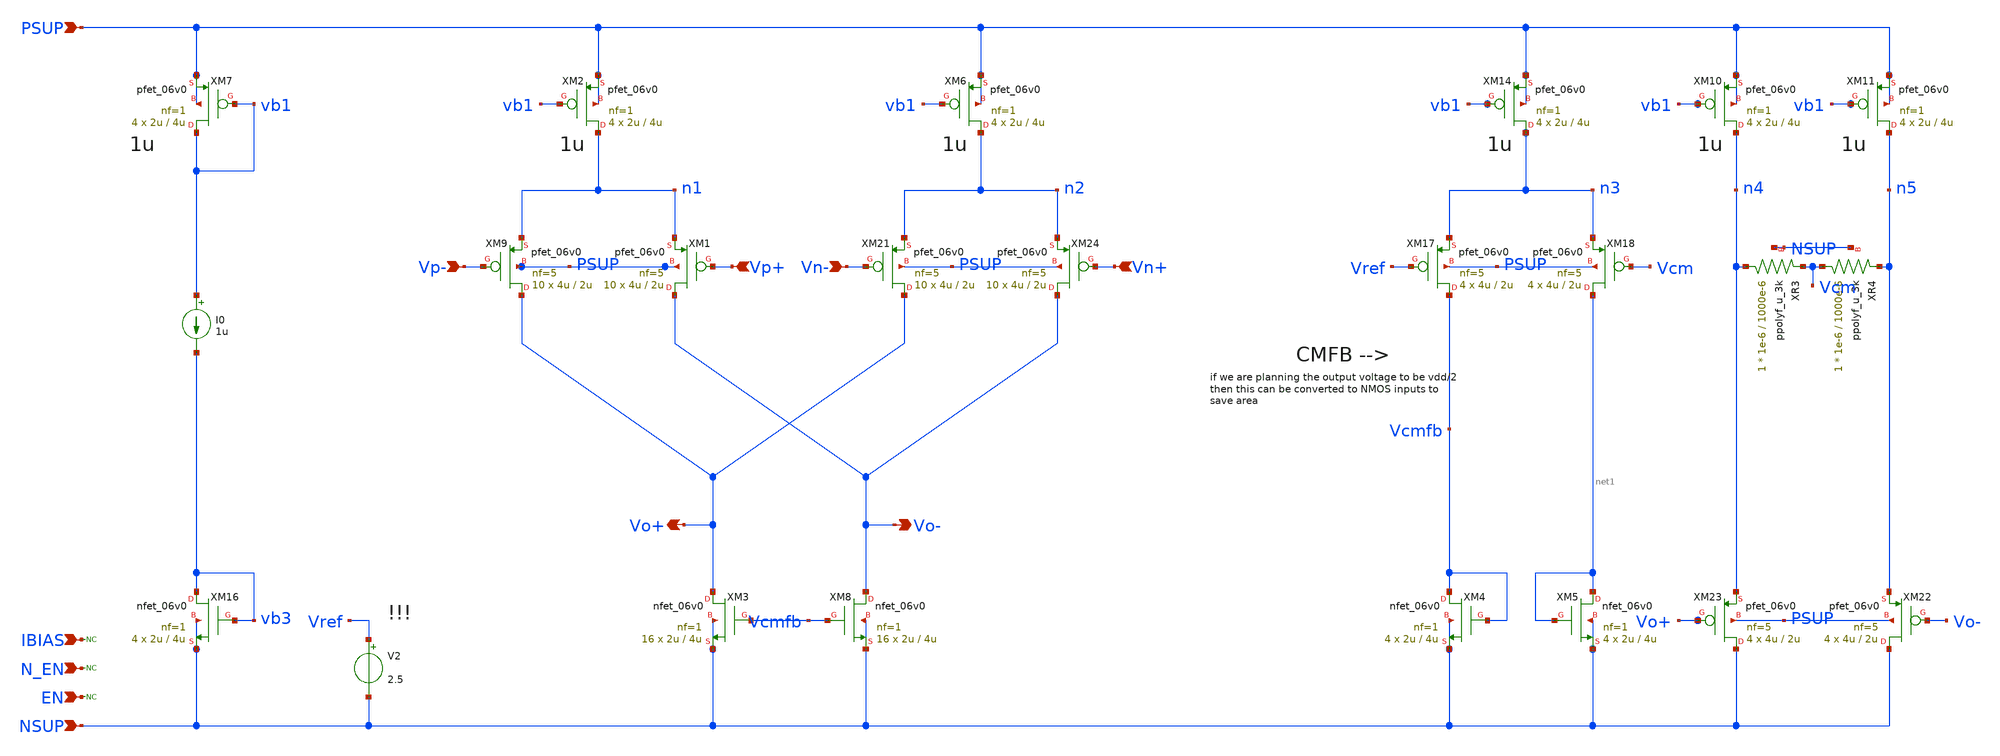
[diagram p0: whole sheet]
** sch_path: xschem/blocks/fdda/junk/fdda_no_casc.sch
**.subckt fdda_no_casc PSUP NSUP N_EN EN IBIAS Vp+ Vp- Vn+ Vn- Vo- Vo+
*.ipin PSUP
*.ipin NSUP
*.ipin N_EN
*.ipin EN
*.ipin IBIAS
*.ipin Vp+
*.ipin Vp-
*.ipin Vn+
*.ipin Vn-
*.opin Vo-
*.opin Vo+
* noconn N_EN
* noconn EN
I0 vb1 vb3 1u
XM7 vb1 vb1 PSUP PSUP pfet_06v0 L=4u W=2u nf=1 ad='int((nf+1)/2) * W/nf * 0.18u' as='int((nf+2)/2) * W/nf * 0.18u'
+ pd='2*int((nf+1)/2) * (W/nf + 0.18u)' ps='2*int((nf+2)/2) * (W/nf + 0.18u)' nrd='0.18u / W' nrs='0.18u / W'
+ sa=0 sb=0 sd=0 m=4
* noconn IBIAS
XM16 vb3 vb3 NSUP NSUP nfet_06v0 L=4u W=2u nf=1 ad='int((nf+1)/2) * W/nf * 0.18u' as='int((nf+2)/2) * W/nf * 0.18u'
+ pd='2*int((nf+1)/2) * (W/nf + 0.18u)' ps='2*int((nf+2)/2) * (W/nf + 0.18u)' nrd='0.18u / W' nrs='0.18u / W'
+ sa=0 sb=0 sd=0 m=4
V2 Vref NSUP 2.5
XM22 NSUP Vo- n5 PSUP pfet_06v0 L=2u W=4u nf=5 ad='int((nf+1)/2) * W/nf * 0.18u' as='int((nf+2)/2) * W/nf * 0.18u'
+ pd='2*int((nf+1)/2) * (W/nf + 0.18u)' ps='2*int((nf+2)/2) * (W/nf + 0.18u)' nrd='0.18u / W' nrs='0.18u / W'
+ sa=0 sb=0 sd=0 m=4
XM23 NSUP Vo+ n4 PSUP pfet_06v0 L=2u W=4u nf=5 ad='int((nf+1)/2) * W/nf * 0.18u' as='int((nf+2)/2) * W/nf * 0.18u'
+ pd='2*int((nf+1)/2) * (W/nf + 0.18u)' ps='2*int((nf+2)/2) * (W/nf + 0.18u)' nrd='0.18u / W' nrs='0.18u / W'
+ sa=0 sb=0 sd=0 m=4
XM9 Vo+ Vp- n1 PSUP pfet_06v0 L=2u W=4u nf=5 ad='int((nf+1)/2) * W/nf * 0.18u' as='int((nf+2)/2) * W/nf * 0.18u'
+ pd='2*int((nf+1)/2) * (W/nf + 0.18u)' ps='2*int((nf+2)/2) * (W/nf + 0.18u)' nrd='0.18u / W' nrs='0.18u / W'
+ sa=0 sb=0 sd=0 m=10
XM1 Vo- Vp+ n1 PSUP pfet_06v0 L=2u W=4u nf=5 ad='int((nf+1)/2) * W/nf * 0.18u' as='int((nf+2)/2) * W/nf * 0.18u'
+ pd='2*int((nf+1)/2) * (W/nf + 0.18u)' ps='2*int((nf+2)/2) * (W/nf + 0.18u)' nrd='0.18u / W' nrs='0.18u / W'
+ sa=0 sb=0 sd=0 m=10
XM2 n1 vb1 PSUP PSUP pfet_06v0 L=4u W=2u nf=1 ad='int((nf+1)/2) * W/nf * 0.18u' as='int((nf+2)/2) * W/nf * 0.18u'
+ pd='2*int((nf+1)/2) * (W/nf + 0.18u)' ps='2*int((nf+2)/2) * (W/nf + 0.18u)' nrd='0.18u / W' nrs='0.18u / W'
+ sa=0 sb=0 sd=0 m=4
XM3 Vo+ Vcmfb NSUP NSUP nfet_06v0 L=4u W=2u nf=1 ad='int((nf+1)/2) * W/nf * 0.18u' as='int((nf+2)/2) * W/nf * 0.18u'
+ pd='2*int((nf+1)/2) * (W/nf + 0.18u)' ps='2*int((nf+2)/2) * (W/nf + 0.18u)' nrd='0.18u / W' nrs='0.18u / W'
+ sa=0 sb=0 sd=0 m=16
XM6 n2 vb1 PSUP PSUP pfet_06v0 L=4u W=2u nf=1 ad='int((nf+1)/2) * W/nf * 0.18u' as='int((nf+2)/2) * W/nf * 0.18u'
+ pd='2*int((nf+1)/2) * (W/nf + 0.18u)' ps='2*int((nf+2)/2) * (W/nf + 0.18u)' nrd='0.18u / W' nrs='0.18u / W'
+ sa=0 sb=0 sd=0 m=4
XM8 Vo- Vcmfb NSUP NSUP nfet_06v0 L=4u W=2u nf=1 ad='int((nf+1)/2) * W/nf * 0.18u' as='int((nf+2)/2) * W/nf * 0.18u'
+ pd='2*int((nf+1)/2) * (W/nf + 0.18u)' ps='2*int((nf+2)/2) * (W/nf + 0.18u)' nrd='0.18u / W' nrs='0.18u / W'
+ sa=0 sb=0 sd=0 m=16
XM4 Vcmfb Vcmfb NSUP NSUP nfet_06v0 L=4u W=2u nf=1 ad='int((nf+1)/2) * W/nf * 0.18u' as='int((nf+2)/2) * W/nf * 0.18u'
+ pd='2*int((nf+1)/2) * (W/nf + 0.18u)' ps='2*int((nf+2)/2) * (W/nf + 0.18u)' nrd='0.18u / W' nrs='0.18u / W'
+ sa=0 sb=0 sd=0 m=4
XM5 net1 net1 NSUP NSUP nfet_06v0 L=4u W=2u nf=1 ad='int((nf+1)/2) * W/nf * 0.18u' as='int((nf+2)/2) * W/nf * 0.18u'
+ pd='2*int((nf+1)/2) * (W/nf + 0.18u)' ps='2*int((nf+2)/2) * (W/nf + 0.18u)' nrd='0.18u / W' nrs='0.18u / W'
+ sa=0 sb=0 sd=0 m=4
XM14 n3 vb1 PSUP PSUP pfet_06v0 L=4u W=2u nf=1 ad='int((nf+1)/2) * W/nf * 0.18u' as='int((nf+2)/2) * W/nf * 0.18u'
+ pd='2*int((nf+1)/2) * (W/nf + 0.18u)' ps='2*int((nf+2)/2) * (W/nf + 0.18u)' nrd='0.18u / W' nrs='0.18u / W'
+ sa=0 sb=0 sd=0 m=4
XM17 Vcmfb Vref n3 PSUP pfet_06v0 L=2u W=4u nf=5 ad='int((nf+1)/2) * W/nf * 0.18u' as='int((nf+2)/2) * W/nf * 0.18u'
+ pd='2*int((nf+1)/2) * (W/nf + 0.18u)' ps='2*int((nf+2)/2) * (W/nf + 0.18u)' nrd='0.18u / W' nrs='0.18u / W'
+ sa=0 sb=0 sd=0 m=4
XM18 net1 Vcm n3 PSUP pfet_06v0 L=2u W=4u nf=5 ad='int((nf+1)/2) * W/nf * 0.18u' as='int((nf+2)/2) * W/nf * 0.18u'
+ pd='2*int((nf+1)/2) * (W/nf + 0.18u)' ps='2*int((nf+2)/2) * (W/nf + 0.18u)' nrd='0.18u / W' nrs='0.18u / W'
+ sa=0 sb=0 sd=0 m=4
XM21 Vo+ Vn- n2 PSUP pfet_06v0 L=2u W=4u nf=5 ad='int((nf+1)/2) * W/nf * 0.18u' as='int((nf+2)/2) * W/nf * 0.18u'
+ pd='2*int((nf+1)/2) * (W/nf + 0.18u)' ps='2*int((nf+2)/2) * (W/nf + 0.18u)' nrd='0.18u / W' nrs='0.18u / W'
+ sa=0 sb=0 sd=0 m=10
XM24 Vo- Vn+ n2 PSUP pfet_06v0 L=2u W=4u nf=5 ad='int((nf+1)/2) * W/nf * 0.18u' as='int((nf+2)/2) * W/nf * 0.18u'
+ pd='2*int((nf+1)/2) * (W/nf + 0.18u)' ps='2*int((nf+2)/2) * (W/nf + 0.18u)' nrd='0.18u / W' nrs='0.18u / W'
+ sa=0 sb=0 sd=0 m=10
XR3 n4 Vcm NSUP ppolyf_u_3k r_width=1e-6 r_length=1000e-6 m=1
XR4 Vcm n5 NSUP ppolyf_u_3k r_width=1e-6 r_length=1000e-6 m=1
XM10 n4 vb1 PSUP PSUP pfet_06v0 L=4u W=2u nf=1 ad='int((nf+1)/2) * W/nf * 0.18u' as='int((nf+2)/2) * W/nf * 0.18u'
+ pd='2*int((nf+1)/2) * (W/nf + 0.18u)' ps='2*int((nf+2)/2) * (W/nf + 0.18u)' nrd='0.18u / W' nrs='0.18u / W'
+ sa=0 sb=0 sd=0 m=4
XM11 n5 vb1 PSUP PSUP pfet_06v0 L=4u W=2u nf=1 ad='int((nf+1)/2) * W/nf * 0.18u' as='int((nf+2)/2) * W/nf * 0.18u'
+ pd='2*int((nf+1)/2) * (W/nf + 0.18u)' ps='2*int((nf+2)/2) * (W/nf + 0.18u)' nrd='0.18u / W' nrs='0.18u / W'
+ sa=0 sb=0 sd=0 m=4
**.ends
.end
